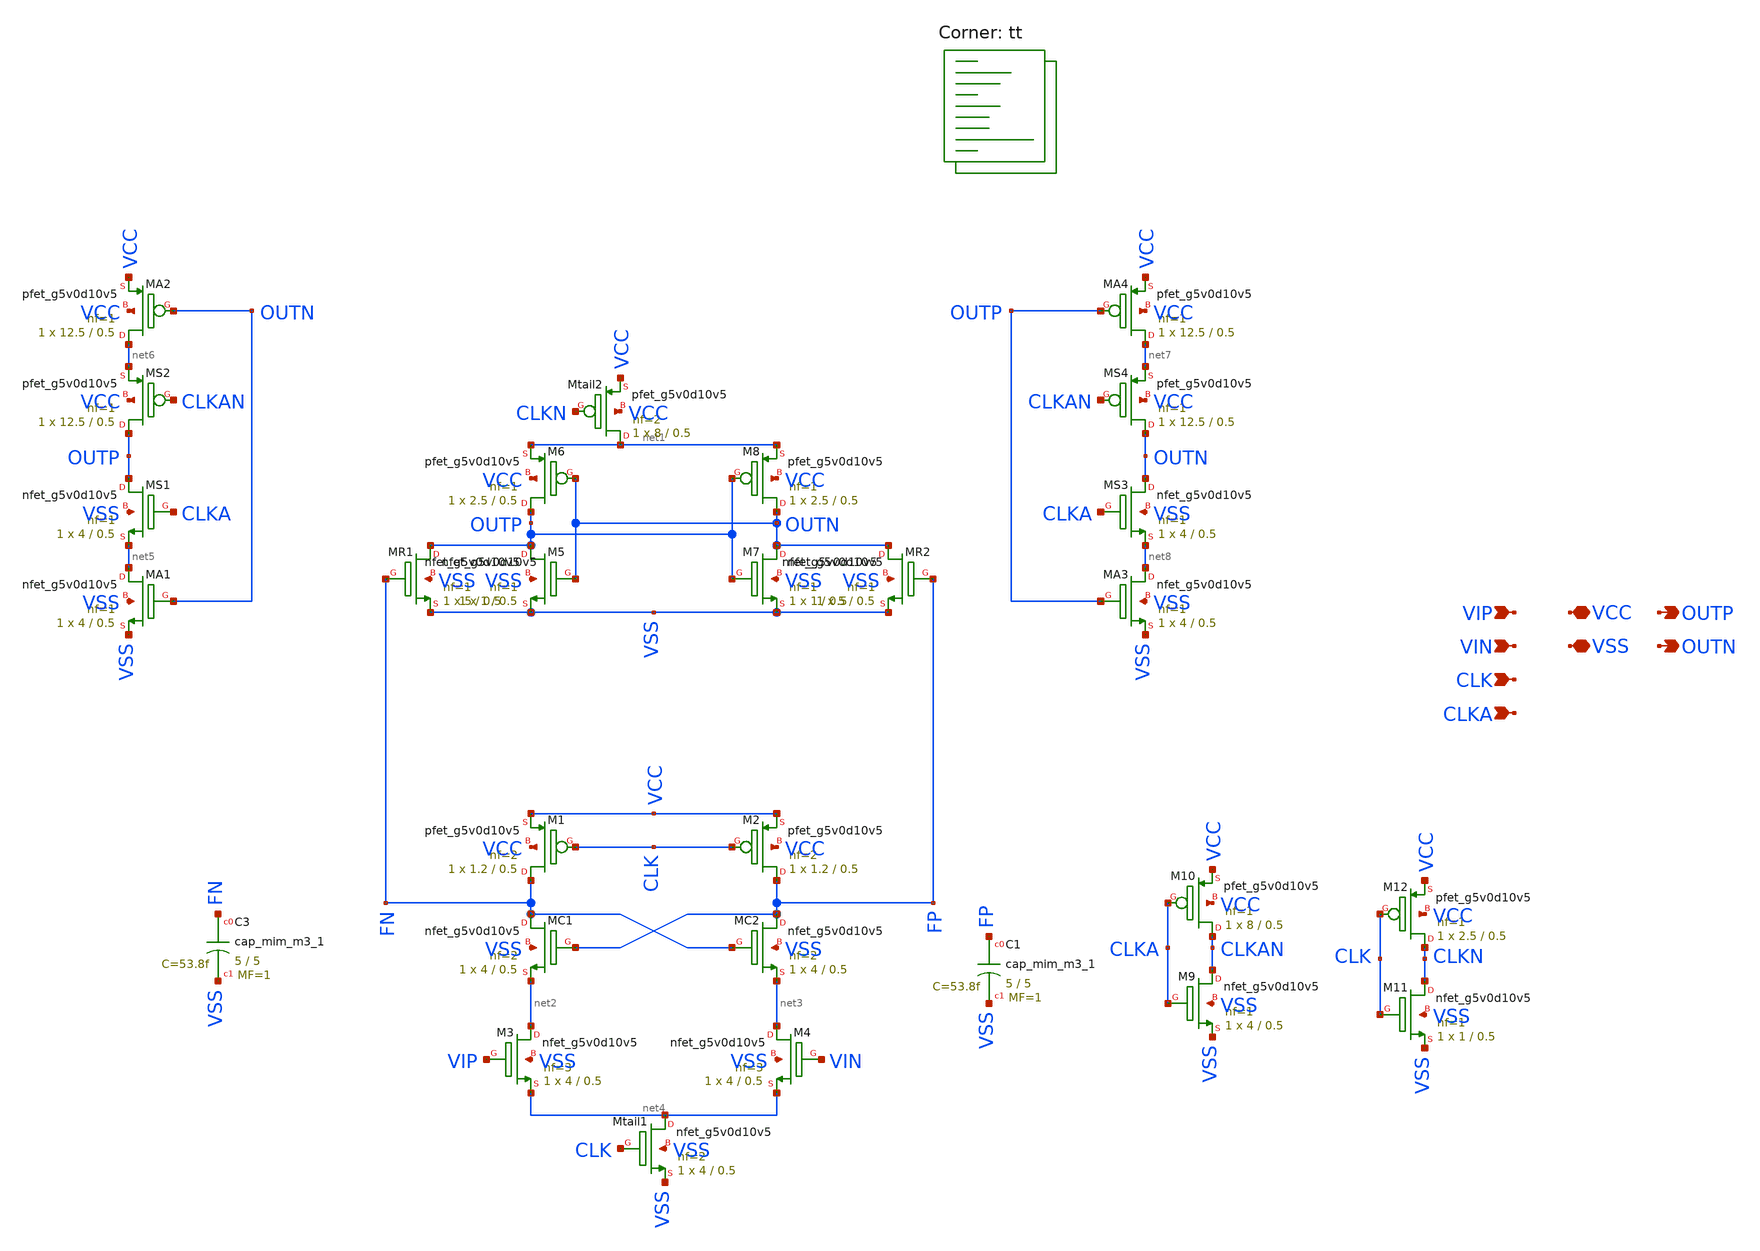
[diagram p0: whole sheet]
** sch_path: Comparator/schematic/new_comparator/miyahara_comparator.sch
**.subckt miyahara_comparator VIP VIN CLK CLKA VCC VSS OUTP OUTN
*.ipin VIP
*.ipin VIN
*.ipin CLK
*.ipin CLKA
*.iopin VCC
*.iopin VSS
*.opin OUTP
*.opin OUTN
XM7 OUTN OUTP VSS VSS sky130_fd_pr__nfet_g5v0d10v5 L=0.5 W=1 nf=1 ad='int((nf+1)/2) * W/nf * 0.29' as='int((nf+2)/2) * W/nf * 0.29'
+ pd='2*int((nf+1)/2) * (W/nf + 0.29)' ps='2*int((nf+2)/2) * (W/nf + 0.29)' nrd='0.29 / W' nrs='0.29 / W'
+ sa=0 sb=0 sd=0 mult=1 m=1
XM8 OUTN OUTP net1 VCC sky130_fd_pr__pfet_g5v0d10v5 L=0.5 W=2.5 nf=1 ad='int((nf+1)/2) * W/nf * 0.29'
+ as='int((nf+2)/2) * W/nf * 0.29' pd='2*int((nf+1)/2) * (W/nf + 0.29)' ps='2*int((nf+2)/2) * (W/nf + 0.29)'
+ nrd='0.29 / W' nrs='0.29 / W' sa=0 sb=0 sd=0 mult=1 m=1
XM5 OUTP OUTN VSS VSS sky130_fd_pr__nfet_g5v0d10v5 L=0.5 W=1 nf=1 ad='int((nf+1)/2) * W/nf * 0.29' as='int((nf+2)/2) * W/nf * 0.29'
+ pd='2*int((nf+1)/2) * (W/nf + 0.29)' ps='2*int((nf+2)/2) * (W/nf + 0.29)' nrd='0.29 / W' nrs='0.29 / W'
+ sa=0 sb=0 sd=0 mult=1 m=1
XM6 OUTP OUTN net1 VCC sky130_fd_pr__pfet_g5v0d10v5 L=0.5 W=2.5 nf=1 ad='int((nf+1)/2) * W/nf * 0.29'
+ as='int((nf+2)/2) * W/nf * 0.29' pd='2*int((nf+1)/2) * (W/nf + 0.29)' ps='2*int((nf+2)/2) * (W/nf + 0.29)'
+ nrd='0.29 / W' nrs='0.29 / W' sa=0 sb=0 sd=0 mult=1 m=1
XMR1 OUTP FN VSS VSS sky130_fd_pr__nfet_g5v0d10v5 L=0.5 W=5 nf=1 ad='int((nf+1)/2) * W/nf * 0.29' as='int((nf+2)/2) * W/nf * 0.29'
+ pd='2*int((nf+1)/2) * (W/nf + 0.29)' ps='2*int((nf+2)/2) * (W/nf + 0.29)' nrd='0.29 / W' nrs='0.29 / W'
+ sa=0 sb=0 sd=0 mult=1 m=1
XMR2 OUTN FP VSS VSS sky130_fd_pr__nfet_g5v0d10v5 L=0.5 W=5 nf=1 ad='int((nf+1)/2) * W/nf * 0.29' as='int((nf+2)/2) * W/nf * 0.29'
+ pd='2*int((nf+1)/2) * (W/nf + 0.29)' ps='2*int((nf+2)/2) * (W/nf + 0.29)' nrd='0.29 / W' nrs='0.29 / W'
+ sa=0 sb=0 sd=0 mult=1 m=1
XMtail2 net1 CLKN VCC VCC sky130_fd_pr__pfet_g5v0d10v5 L=0.5 W=8 nf=2 ad='int((nf+1)/2) * W/nf * 0.29'
+ as='int((nf+2)/2) * W/nf * 0.29' pd='2*int((nf+1)/2) * (W/nf + 0.29)' ps='2*int((nf+2)/2) * (W/nf + 0.29)'
+ nrd='0.29 / W' nrs='0.29 / W' sa=0 sb=0 sd=0 mult=1 m=1
XM2 FP CLK VCC VCC sky130_fd_pr__pfet_g5v0d10v5 L=0.5 W=1.2 nf=2 ad='int((nf+1)/2) * W/nf * 0.29' as='int((nf+2)/2) * W/nf * 0.29'
+ pd='2*int((nf+1)/2) * (W/nf + 0.29)' ps='2*int((nf+2)/2) * (W/nf + 0.29)' nrd='0.29 / W' nrs='0.29 / W'
+ sa=0 sb=0 sd=0 mult=1 m=1
XM1 FN CLK VCC VCC sky130_fd_pr__pfet_g5v0d10v5 L=0.5 W=1.2 nf=2 ad='int((nf+1)/2) * W/nf * 0.29' as='int((nf+2)/2) * W/nf * 0.29'
+ pd='2*int((nf+1)/2) * (W/nf + 0.29)' ps='2*int((nf+2)/2) * (W/nf + 0.29)' nrd='0.29 / W' nrs='0.29 / W'
+ sa=0 sb=0 sd=0 mult=1 m=1
XMC2 FP FN net3 VSS sky130_fd_pr__nfet_g5v0d10v5 L=0.5 W=4 nf=2 ad='int((nf+1)/2) * W/nf * 0.29' as='int((nf+2)/2) * W/nf * 0.29'
+ pd='2*int((nf+1)/2) * (W/nf + 0.29)' ps='2*int((nf+2)/2) * (W/nf + 0.29)' nrd='0.29 / W' nrs='0.29 / W'
+ sa=0 sb=0 sd=0 mult=1 m=1
XMC1 FN FP net2 VSS sky130_fd_pr__nfet_g5v0d10v5 L=0.5 W=4 nf=2 ad='int((nf+1)/2) * W/nf * 0.29' as='int((nf+2)/2) * W/nf * 0.29'
+ pd='2*int((nf+1)/2) * (W/nf + 0.29)' ps='2*int((nf+2)/2) * (W/nf + 0.29)' nrd='0.29 / W' nrs='0.29 / W'
+ sa=0 sb=0 sd=0 mult=1 m=1
XM4 net3 VIN net4 VSS sky130_fd_pr__nfet_g5v0d10v5 L=0.5 W=4 nf=3 ad='int((nf+1)/2) * W/nf * 0.29' as='int((nf+2)/2) * W/nf * 0.29'
+ pd='2*int((nf+1)/2) * (W/nf + 0.29)' ps='2*int((nf+2)/2) * (W/nf + 0.29)' nrd='0.29 / W' nrs='0.29 / W'
+ sa=0 sb=0 sd=0 mult=1 m=1
XM3 net2 VIP net4 VSS sky130_fd_pr__nfet_g5v0d10v5 L=0.5 W=4 nf=3 ad='int((nf+1)/2) * W/nf * 0.29' as='int((nf+2)/2) * W/nf * 0.29'
+ pd='2*int((nf+1)/2) * (W/nf + 0.29)' ps='2*int((nf+2)/2) * (W/nf + 0.29)' nrd='0.29 / W' nrs='0.29 / W'
+ sa=0 sb=0 sd=0 mult=1 m=1
XMtail1 net4 CLK VSS VSS sky130_fd_pr__nfet_g5v0d10v5 L=0.5 W=4 nf=2 ad='int((nf+1)/2) * W/nf * 0.29'
+ as='int((nf+2)/2) * W/nf * 0.29' pd='2*int((nf+1)/2) * (W/nf + 0.29)' ps='2*int((nf+2)/2) * (W/nf + 0.29)'
+ nrd='0.29 / W' nrs='0.29 / W' sa=0 sb=0 sd=0 mult=1 m=1
XMS1 OUTP CLKA net5 VSS sky130_fd_pr__nfet_g5v0d10v5 L=0.5 W=4 nf=1 ad='int((nf+1)/2) * W/nf * 0.29'
+ as='int((nf+2)/2) * W/nf * 0.29' pd='2*int((nf+1)/2) * (W/nf + 0.29)' ps='2*int((nf+2)/2) * (W/nf + 0.29)'
+ nrd='0.29 / W' nrs='0.29 / W' sa=0 sb=0 sd=0 mult=1 m=1
XMA2 net6 OUTN VCC VCC sky130_fd_pr__pfet_g5v0d10v5 L=0.5 W=12.5 nf=1 ad='int((nf+1)/2) * W/nf * 0.29'
+ as='int((nf+2)/2) * W/nf * 0.29' pd='2*int((nf+1)/2) * (W/nf + 0.29)' ps='2*int((nf+2)/2) * (W/nf + 0.29)'
+ nrd='0.29 / W' nrs='0.29 / W' sa=0 sb=0 sd=0 mult=1 m=1
XMS2 OUTP CLKAN net6 VCC sky130_fd_pr__pfet_g5v0d10v5 L=0.5 W=12.5 nf=1 ad='int((nf+1)/2) * W/nf * 0.29'
+ as='int((nf+2)/2) * W/nf * 0.29' pd='2*int((nf+1)/2) * (W/nf + 0.29)' ps='2*int((nf+2)/2) * (W/nf + 0.29)'
+ nrd='0.29 / W' nrs='0.29 / W' sa=0 sb=0 sd=0 mult=1 m=1
XMA1 net5 OUTN VSS VSS sky130_fd_pr__nfet_g5v0d10v5 L=0.5 W=4 nf=1 ad='int((nf+1)/2) * W/nf * 0.29' as='int((nf+2)/2) * W/nf * 0.29'
+ pd='2*int((nf+1)/2) * (W/nf + 0.29)' ps='2*int((nf+2)/2) * (W/nf + 0.29)' nrd='0.29 / W' nrs='0.29 / W'
+ sa=0 sb=0 sd=0 mult=1 m=1
XMS3 OUTN CLKA net8 VSS sky130_fd_pr__nfet_g5v0d10v5 L=0.5 W=4 nf=1 ad='int((nf+1)/2) * W/nf * 0.29'
+ as='int((nf+2)/2) * W/nf * 0.29' pd='2*int((nf+1)/2) * (W/nf + 0.29)' ps='2*int((nf+2)/2) * (W/nf + 0.29)'
+ nrd='0.29 / W' nrs='0.29 / W' sa=0 sb=0 sd=0 mult=1 m=1
XMA4 net7 OUTP VCC VCC sky130_fd_pr__pfet_g5v0d10v5 L=0.5 W=12.5 nf=1 ad='int((nf+1)/2) * W/nf * 0.29'
+ as='int((nf+2)/2) * W/nf * 0.29' pd='2*int((nf+1)/2) * (W/nf + 0.29)' ps='2*int((nf+2)/2) * (W/nf + 0.29)'
+ nrd='0.29 / W' nrs='0.29 / W' sa=0 sb=0 sd=0 mult=1 m=1
XMS4 OUTN CLKAN net7 VCC sky130_fd_pr__pfet_g5v0d10v5 L=0.5 W=12.5 nf=1 ad='int((nf+1)/2) * W/nf * 0.29'
+ as='int((nf+2)/2) * W/nf * 0.29' pd='2*int((nf+1)/2) * (W/nf + 0.29)' ps='2*int((nf+2)/2) * (W/nf + 0.29)'
+ nrd='0.29 / W' nrs='0.29 / W' sa=0 sb=0 sd=0 mult=1 m=1
XMA3 net8 OUTP VSS VSS sky130_fd_pr__nfet_g5v0d10v5 L=0.5 W=4 nf=1 ad='int((nf+1)/2) * W/nf * 0.29' as='int((nf+2)/2) * W/nf * 0.29'
+ pd='2*int((nf+1)/2) * (W/nf + 0.29)' ps='2*int((nf+2)/2) * (W/nf + 0.29)' nrd='0.29 / W' nrs='0.29 / W'
+ sa=0 sb=0 sd=0 mult=1 m=1
XM9 CLKAN CLKA VSS VSS sky130_fd_pr__nfet_g5v0d10v5 L=0.5 W=4 nf=1 ad='int((nf+1)/2) * W/nf * 0.29' as='int((nf+2)/2) * W/nf * 0.29'
+ pd='2*int((nf+1)/2) * (W/nf + 0.29)' ps='2*int((nf+2)/2) * (W/nf + 0.29)' nrd='0.29 / W' nrs='0.29 / W'
+ sa=0 sb=0 sd=0 mult=1 m=1
XM10 CLKAN CLKA VCC VCC sky130_fd_pr__pfet_g5v0d10v5 L=0.5 W=8 nf=1 ad='int((nf+1)/2) * W/nf * 0.29'
+ as='int((nf+2)/2) * W/nf * 0.29' pd='2*int((nf+1)/2) * (W/nf + 0.29)' ps='2*int((nf+2)/2) * (W/nf + 0.29)'
+ nrd='0.29 / W' nrs='0.29 / W' sa=0 sb=0 sd=0 mult=1 m=1
XM11 CLKN CLK VSS VSS sky130_fd_pr__nfet_g5v0d10v5 L=0.5 W=1 nf=1 ad='int((nf+1)/2) * W/nf * 0.29' as='int((nf+2)/2) * W/nf * 0.29'
+ pd='2*int((nf+1)/2) * (W/nf + 0.29)' ps='2*int((nf+2)/2) * (W/nf + 0.29)' nrd='0.29 / W' nrs='0.29 / W'
+ sa=0 sb=0 sd=0 mult=1 m=1
XM12 CLKN CLK VCC VCC sky130_fd_pr__pfet_g5v0d10v5 L=0.5 W=2.5 nf=1 ad='int((nf+1)/2) * W/nf * 0.29'
+ as='int((nf+2)/2) * W/nf * 0.29' pd='2*int((nf+1)/2) * (W/nf + 0.29)' ps='2*int((nf+2)/2) * (W/nf + 0.29)'
+ nrd='0.29 / W' nrs='0.29 / W' sa=0 sb=0 sd=0 mult=1 m=1
XC3 FN VSS sky130_fd_pr__cap_mim_m3_1 W=5 L=5 MF=1 m=1
XC1 FP VSS sky130_fd_pr__cap_mim_m3_1 W=5 L=5 MF=1 m=1
**** begin user architecture code



.param ton = 1n

V1 VSS 0 dc 0
V2 VCC 0 dc 3.3
V3 CLK 0 pulse(0 3.3 {ton} 0.01ns 0.01ns {ton} 4ns)
V4 CLKA 0 pulse(0 3.3 {ton*1.5} 0.01ns 0.01ns {ton/2} 4ns)
V5 VIP 0 dc 1.40
V6 VIN 0 dc 1.40

.save all
.tran 0.1n 30n uic
**** interactive sim
.control
run
*set filetype=ascii
write miyahara_comparator.raw vin vip fp fn outp outn clk clka
*plot vin vip RN1 rp1 fp1 fn1
quit
.endc



.lib $::SKYWATER_MODELS/sky130.lib.spice tt
**** end user architecture code
**.ends
.end
